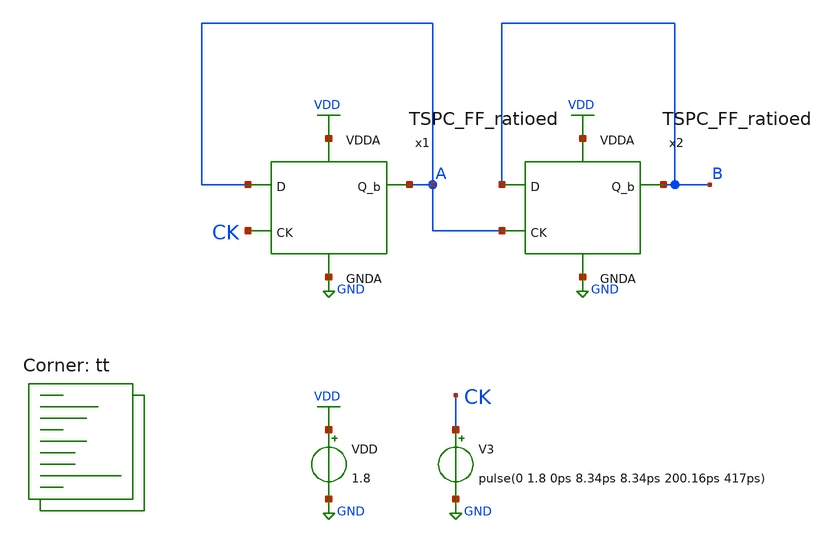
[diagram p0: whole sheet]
** sch_path: projects/pll/divider/xschem_ngspice/tb_TSPC_FF_ratioed.sch
**.subckt tb_TSPC_FF_ratioed
VDD VDD GND 1.8
V3 CK GND pulse(0 1.8 0ps 8.34ps 8.34ps 200.16ps 417ps)
x1 VDD A A CK GND TSPC_FF_ratioed
x2 VDD B B A GND TSPC_FF_ratioed
**** begin user architecture code



.include /foss/pdks/sky130A/libs.ref/sky130_fd_sc_hd/spice/sky130_fd_sc_hd.spice

.option method=gear
.option wnflag=1
* .option savecurrents

.save @m.x1.xm1.msky130_fd_pr__nfet_01v8[gm] @m.x1.xm2.msky130_fd_pr__nfet_01v8[gm] @m.x1.xm3.msky130_fd_pr__pfet_01v8[gm] @m.x1.xm4.msky130_fd_pr__pfet_01v8[gm] @m.x1.xm5.msky130_fd_pr__nfet_01v8[gm] @m.x1.xm6.msky130_fd_pr__nfet_01v8[gm] @m.x1.xm7.msky130_fd_pr__nfet_01v8[gm] @m.x5.xm1.msky130_fd_pr__nfet_01v8[gm] @m.x5.xm2.msky130_fd_pr__nfet_01v8[gm] @m.x5.xm3.msky130_fd_pr__pfet_01v8[gm] @m.x5.xm4.msky130_fd_pr__pfet_01v8[gm] @m.x5.xm5.msky130_fd_pr__nfet_01v8[gm] @m.x5.xm6.msky130_fd_pr__nfet_01v8[gm] @m.x5.xm7.msky130_fd_pr__nfet_01v8[gm] @v.x1.vmeas @v.x1.vmeas1 @v.x1.vmeas2 @v.x5.vmeas @v.x5.vmeas1 @v.x5.vmeas2


.control

  * save v(a) v(a_b) v(b) v(b_b) v(ck)
  save all
  *tran 0.1n 1u
  tran 0.2p 10n

  remzerovec
  write tb_TSPC_FF_ratioed.raw
  set appendwrite

.endc



.lib $::SKYWATER_MODELS/sky130.lib.spice tt
**** end user architecture code
**.ends

* expanding   symbol:
*+  /foss/designs/my_design/projects/pll/divider/xschem_ngspice/TSPC_FF_ratioed.sym # of pins=5
** sym_path: projects/pll/divider/xschem_ngspice/TSPC_FF_ratioed.sym
** sch_path: projects/pll/divider/xschem_ngspice/TSPC_FF_ratioed.sch
.subckt TSPC_FF_ratioed VDDA Q_b D CK GNDA
*.ipin CK
*.ipin D
*.opin Q_b
*.ipin VDDA
*.ipin GNDA
XM1 Q_b CK VDDA VDDA sky130_fd_pr__pfet_01v8 L=0.15 W=1 nf=1 ad='int((nf+1)/2) * W/nf * 0.29' as='int((nf+2)/2) * W/nf * 0.29'
+ pd='2*int((nf+1)/2) * (W/nf + 0.29)' ps='2*int((nf+2)/2) * (W/nf + 0.29)' nrd='0.29 / W' nrs='0.29 / W'
+ sa=0 sb=0 sd=0 mult=1 m=1
XM2 Q_b net2 GNDA GNDA sky130_fd_pr__nfet_01v8 L=0.15 W=1 nf=1 ad='int((nf+1)/2) * W/nf * 0.29' as='int((nf+2)/2) * W/nf * 0.29'
+ pd='2*int((nf+1)/2) * (W/nf + 0.29)' ps='2*int((nf+2)/2) * (W/nf + 0.29)' nrd='0.29 / W' nrs='0.29 / W'
+ sa=0 sb=0 sd=0 mult=1 m=1
XM3 net2 net3 VDDA VDDA sky130_fd_pr__pfet_01v8 L=0.15 W=1 nf=1 ad='int((nf+1)/2) * W/nf * 0.29' as='int((nf+2)/2) * W/nf * 0.29'
+ pd='2*int((nf+1)/2) * (W/nf + 0.29)' ps='2*int((nf+2)/2) * (W/nf + 0.29)' nrd='0.29 / W' nrs='0.29 / W'
+ sa=0 sb=0 sd=0 mult=1 m=1
XM4 net2 CK GNDA GNDA sky130_fd_pr__nfet_01v8 L=0.15 W=3 nf=3 ad='int((nf+1)/2) * W/nf * 0.29' as='int((nf+2)/2) * W/nf * 0.29'
+ pd='2*int((nf+1)/2) * (W/nf + 0.29)' ps='2*int((nf+2)/2) * (W/nf + 0.29)' nrd='0.29 / W' nrs='0.29 / W'
+ sa=0 sb=0 sd=0 mult=1 m=1
XM5 net3 D VDDA VDDA sky130_fd_pr__pfet_01v8 L=0.15 W=1 nf=1 ad='int((nf+1)/2) * W/nf * 0.29' as='int((nf+2)/2) * W/nf * 0.29'
+ pd='2*int((nf+1)/2) * (W/nf + 0.29)' ps='2*int((nf+2)/2) * (W/nf + 0.29)' nrd='0.29 / W' nrs='0.29 / W'
+ sa=0 sb=0 sd=0 mult=1 m=1
XM7 net1 D GNDA GNDA sky130_fd_pr__nfet_01v8 L=0.15 W=1 nf=1 ad='int((nf+1)/2) * W/nf * 0.29' as='int((nf+2)/2) * W/nf * 0.29'
+ pd='2*int((nf+1)/2) * (W/nf + 0.29)' ps='2*int((nf+2)/2) * (W/nf + 0.29)' nrd='0.29 / W' nrs='0.29 / W'
+ sa=0 sb=0 sd=0 mult=1 m=1
XM6 net3 CK net1 GNDA sky130_fd_pr__nfet_01v8 L=0.15 W=1 nf=1 ad='int((nf+1)/2) * W/nf * 0.29' as='int((nf+2)/2) * W/nf * 0.29'
+ pd='2*int((nf+1)/2) * (W/nf + 0.29)' ps='2*int((nf+2)/2) * (W/nf + 0.29)' nrd='0.29 / W' nrs='0.29 / W'
+ sa=0 sb=0 sd=0 mult=1 m=1
.ends

.GLOBAL GND
.GLOBAL VDD
.end
